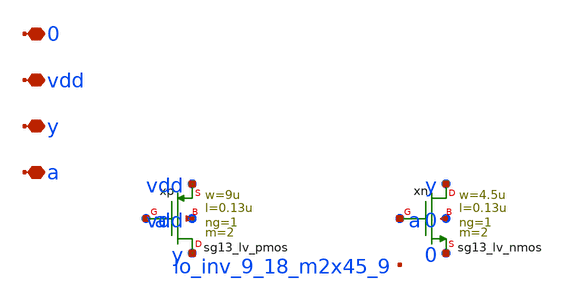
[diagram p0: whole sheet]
** sch_path: analog/lo/sch/lo_inv_9_18.sch
**.subckt lo_inv_9_18 a y vdd 0
*.iopin a
*.iopin y
*.iopin vdd
*.iopin 0
Xxp y a vdd vdd sg13_lv_pmos w=9u l=0.13u ng=1 m=2 mm_ok=1
Xxn y a 0 0 sg13_lv_nmos w=4.5u l=0.13u ng=1 m=2 mm_ok=1
**.ends
.end
